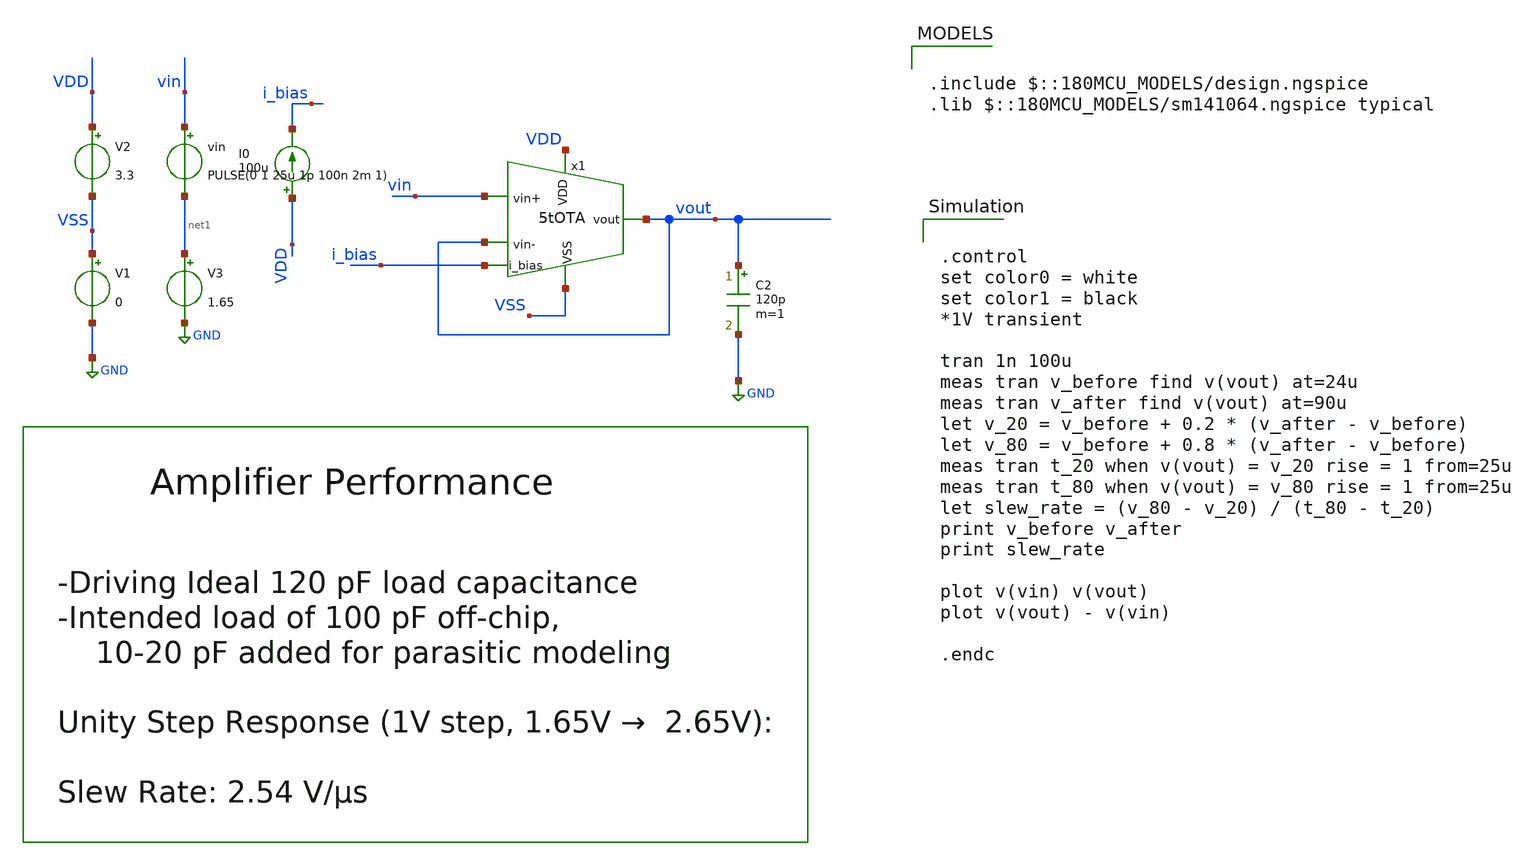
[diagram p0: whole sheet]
** sch_path: designs/libs/core_amps/ota_5t/tb/5tOTA_tb_tran_SR.sch
**.subckt 5tOTA_tb_tran_SR
V1 VSS GND 0
V2 VDD VSS 3.3
I0 VDD i_bias 100u
vin vin net1 PULSE(0 1 25u 1p 100n 2m 1)
C2 vout GND 120p m=1
V3 net1 GND 1.65
x1 VDD vout vin vout i_bias VSS 5tOTA
**** begin user architecture code

.include $::180MCU_MODELS/design.ngspice
.lib $::180MCU_MODELS/sm141064.ngspice typical



.control
set color0 = white
set color1 = black
*1V transient

tran 1n 100u
meas tran v_before find v(vout) at=24u
meas tran v_after find v(vout) at=90u
let v_20 = v_before + 0.2 * (v_after - v_before)
let v_80 = v_before + 0.8 * (v_after - v_before)
meas tran t_20 when v(vout) = v_20 rise = 1 from=25u
meas tran t_80 when v(vout) = v_80 rise = 1 from=25u
let slew_rate = (v_80 - v_20) / (t_80 - t_20)
print v_before v_after
print slew_rate

plot v(vin) v(vout)
plot v(vout) - v(vin)

.endc


**** end user architecture code
**.ends

* expanding   symbol:  libs/core_amps/ota_5t/schem/5tOTA.sym # of pins=6
** sym_path: designs/5tOTA.sym
** sch_path: designs/5tOTA.sch
.subckt 5tOTA VDD vout vin+ vin- i_bias VSS
*.ipin VDD
*.opin vout
*.ipin i_bias
*.ipin vin+
*.ipin vin-
*.ipin VSS
XM1 net1 vin+ net2 VSS nfet_03v3 L=0.5u W=11.43u nf=1 ad='int((nf+1)/2) * W/nf * 0.18u' as='int((nf+2)/2) * W/nf * 0.18u'
+ pd='2*int((nf+1)/2) * (W/nf + 0.18u)' ps='2*int((nf+2)/2) * (W/nf + 0.18u)' nrd='0.18u / W' nrs='0.18u / W'
+ sa=0 sb=0 sd=0 m=1
XM2 vout vin- net2 VSS nfet_03v3 L=0.5u W=11.43u nf=1 ad='int((nf+1)/2) * W/nf * 0.18u' as='int((nf+2)/2) * W/nf * 0.18u'
+ pd='2*int((nf+1)/2) * (W/nf + 0.18u)' ps='2*int((nf+2)/2) * (W/nf + 0.18u)' nrd='0.18u / W' nrs='0.18u / W'
+ sa=0 sb=0 sd=0 m=1
XM3 net1 net1 VDD VDD pfet_03v3 L=0.5u W=22.86u nf=1 ad='int((nf+1)/2) * W/nf * 0.18u' as='int((nf+2)/2) * W/nf * 0.18u'
+ pd='2*int((nf+1)/2) * (W/nf + 0.18u)' ps='2*int((nf+2)/2) * (W/nf + 0.18u)' nrd='0.18u / W' nrs='0.18u / W'
+ sa=0 sb=0 sd=0 m=1
XM4 vout net1 VDD VDD pfet_03v3 L=0.5u W=22.86u nf=1 ad='int((nf+1)/2) * W/nf * 0.18u' as='int((nf+2)/2) * W/nf * 0.18u'
+ pd='2*int((nf+1)/2) * (W/nf + 0.18u)' ps='2*int((nf+2)/2) * (W/nf + 0.18u)' nrd='0.18u / W' nrs='0.18u / W'
+ sa=0 sb=0 sd=0 m=1
XM5 net2 i_bias VSS VSS nfet_03v3 L=0.5u W=22.86u nf=1 ad='int((nf+1)/2) * W/nf * 0.18u' as='int((nf+2)/2) * W/nf * 0.18u'
+ pd='2*int((nf+1)/2) * (W/nf + 0.18u)' ps='2*int((nf+2)/2) * (W/nf + 0.18u)' nrd='0.18u / W' nrs='0.18u / W'
+ sa=0 sb=0 sd=0 m=1
XM6 i_bias i_bias VSS VSS nfet_03v3 L=0.5u W=22.86u nf=1 ad='int((nf+1)/2) * W/nf * 0.18u' as='int((nf+2)/2) * W/nf * 0.18u'
+ pd='2*int((nf+1)/2) * (W/nf + 0.18u)' ps='2*int((nf+2)/2) * (W/nf + 0.18u)' nrd='0.18u / W' nrs='0.18u / W'
+ sa=0 sb=0 sd=0 m=1
.ends

.GLOBAL GND
.end
